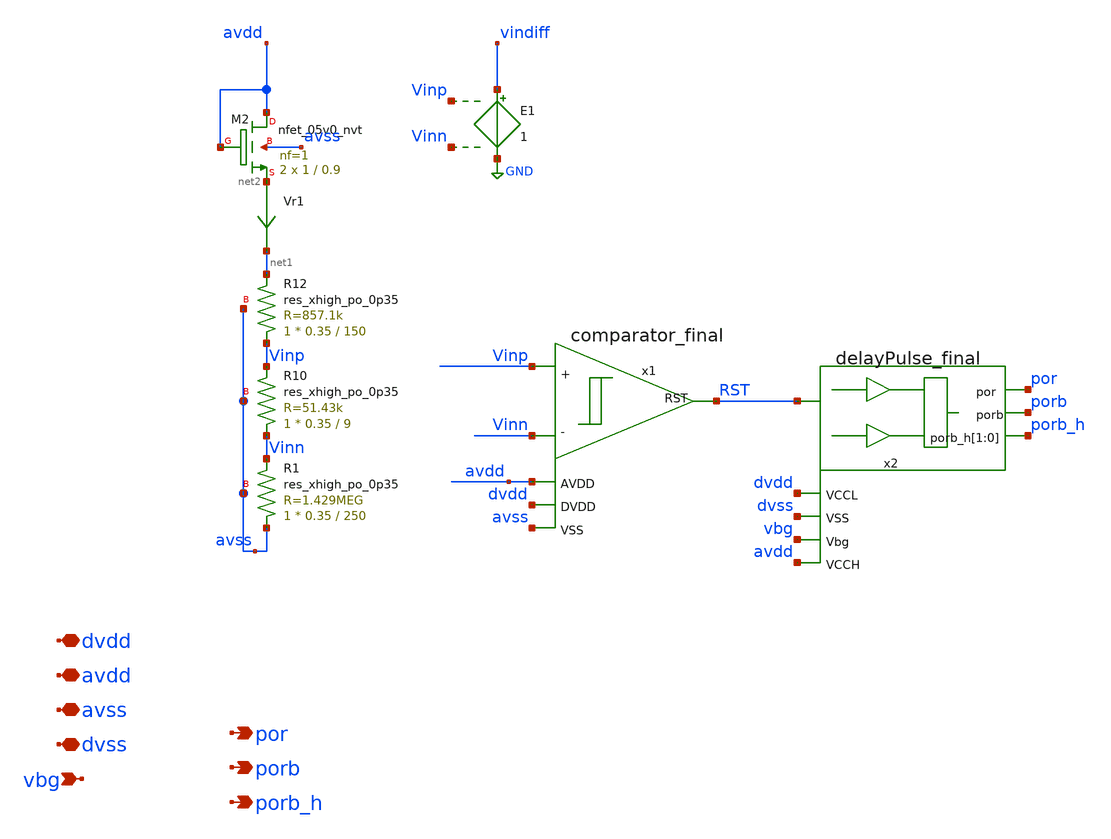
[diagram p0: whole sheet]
** sch_path: xschem/sky130_sw_ip__bgrref_por.sch
**.subckt sky130_sw_ip__bgrref_por avdd por avss dvdd porb vbg porb_h dvss
*.iopin avdd
*.opin por
*.iopin avss
*.iopin dvdd
*.opin porb
*.ipin vbg
*.opin porb_h
*.iopin dvss
Vr1 net2 net1 0
.save i(vr1)
E1 vindiff GND Vinp Vinn 1
x1 Vinn Vinp RST avss avdd dvdd comparator_final
XR1 avss Vinn avss sky130_fd_pr__res_xhigh_po_0p35 L=250 mult=1 m=1
XR10 Vinn Vinp avss sky130_fd_pr__res_xhigh_po_0p35 L=9 mult=1 m=1
XR12 Vinp net1 avss sky130_fd_pr__res_xhigh_po_0p35 L=150 mult=1 m=1
x2 RST por dvdd dvss vbg avdd porb porb_h porb_h delayPulse_final
XM2 avdd avdd net2 avss sky130_fd_pr__nfet_05v0_nvt L=0.9 W=1 nf=1 ad='int((nf+1)/2) * W/nf * 0.29' as='int((nf+2)/2) * W/nf * 0.29'
+ pd='2*int((nf+1)/2) * (W/nf + 0.29)' ps='2*int((nf+2)/2) * (W/nf + 0.29)' nrd='0.29 / W' nrs='0.29 / W'
+ sa=0 sb=0 sd=0 mult=2 m=2
**.ends
.GLOBAL GND
.end
